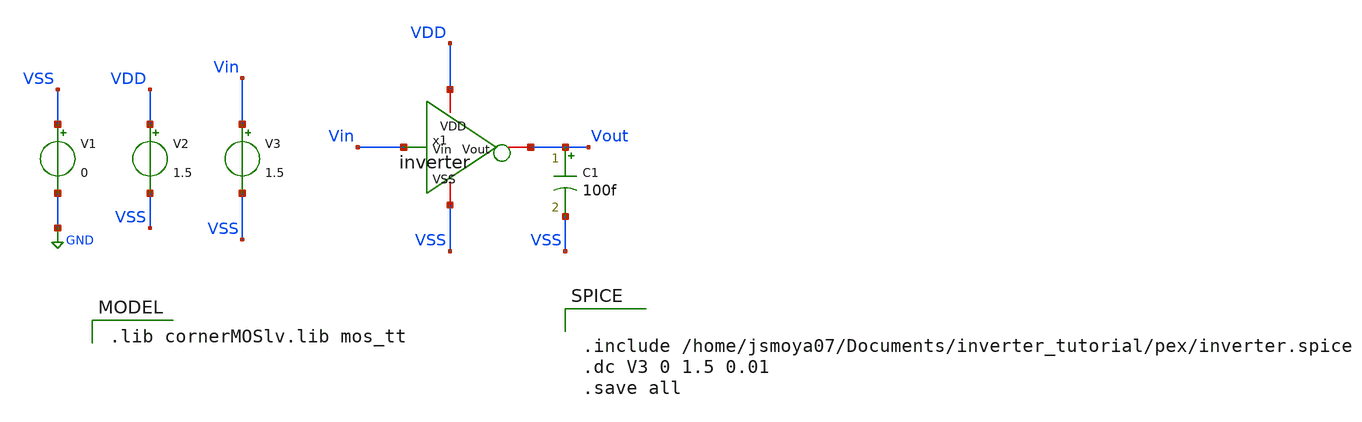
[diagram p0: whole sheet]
** sch_path: inverter_tutorial/pex/inverter_tb.sch
**.subckt inverter_tb
C1 Vout VSS 100f m=1
V1 VSS GND 0
V2 VDD VSS 1.5
V3 Vin VSS 1.5
x1 VDD Vout Vin VSS inverter
**** begin user architecture code
 .lib cornerMOSlv.lib mos_tt



.include /home/jsmoya07/Documents/inverter_tutorial/pex/inverter.spice
.dc V3 0 1.5 0.01
.save all


**** end user architecture code
**.ends
.GLOBAL GND
.end
